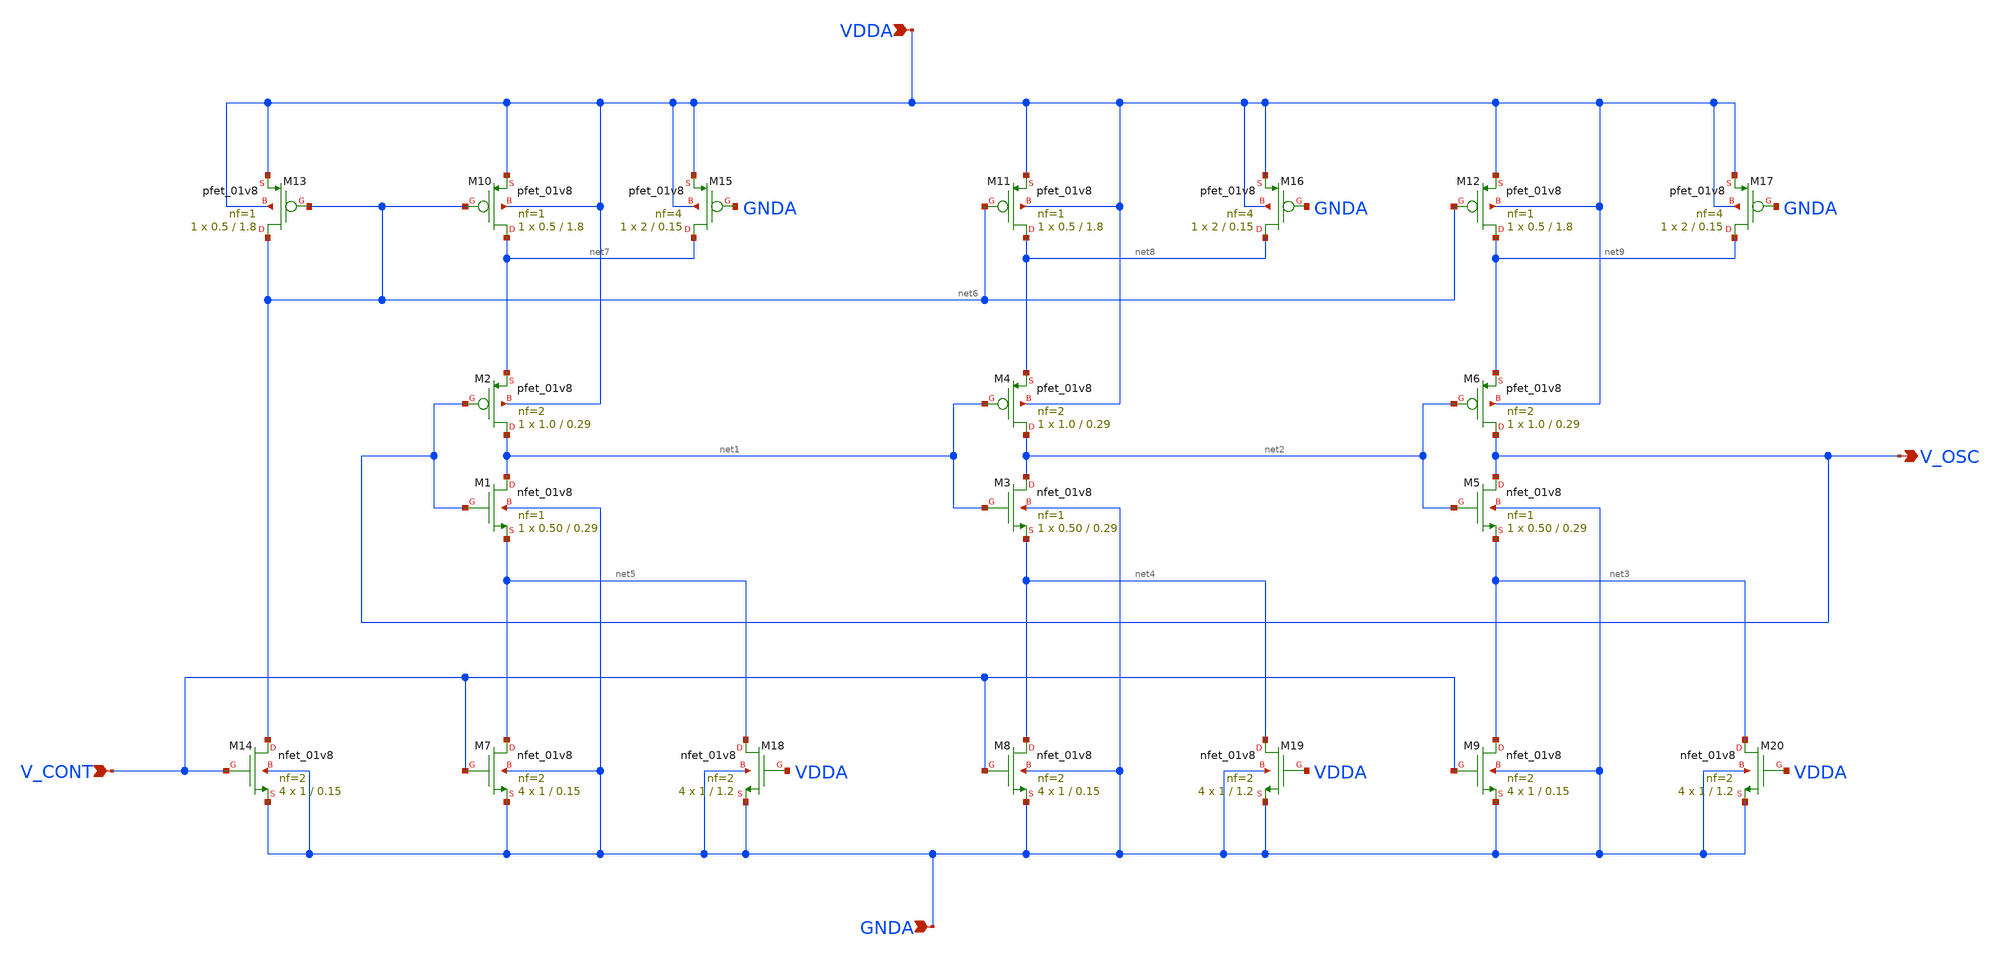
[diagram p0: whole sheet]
** sch_path: projects/pll/vco/xschem_ngspice/current_starved_VCO.sch
**.subckt current_starved_VCO VDDA V_OSC GNDA V_CONT
*.ipin VDDA
*.opin V_OSC
*.ipin GNDA
*.ipin V_CONT
XM1 net1 V_OSC net5 GNDA sky130_fd_pr__nfet_01v8 L=0.29 W=0.50 nf=1 ad='int((nf+1)/2) * W/nf * 0.29'
+ as='int((nf+2)/2) * W/nf * 0.29' pd='2*int((nf+1)/2) * (W/nf + 0.29)' ps='2*int((nf+2)/2) * (W/nf + 0.29)'
+ nrd='0.29 / W' nrs='0.29 / W' sa=0 sb=0 sd=0 mult=1 m=1
XM2 net1 V_OSC net7 VDDA sky130_fd_pr__pfet_01v8 L=0.29 W=1.0 nf=2 ad='int((nf+1)/2) * W/nf * 0.29' as='int((nf+2)/2) * W/nf * 0.29'
+ pd='2*int((nf+1)/2) * (W/nf + 0.29)' ps='2*int((nf+2)/2) * (W/nf + 0.29)' nrd='0.29 / W' nrs='0.29 / W'
+ sa=0 sb=0 sd=0 mult=1 m=1
XM3 net2 net1 net4 GNDA sky130_fd_pr__nfet_01v8 L=0.29 W=0.50 nf=1 ad='int((nf+1)/2) * W/nf * 0.29' as='int((nf+2)/2) * W/nf * 0.29'
+ pd='2*int((nf+1)/2) * (W/nf + 0.29)' ps='2*int((nf+2)/2) * (W/nf + 0.29)' nrd='0.29 / W' nrs='0.29 / W'
+ sa=0 sb=0 sd=0 mult=1 m=1
XM4 net2 net1 net8 VDDA sky130_fd_pr__pfet_01v8 L=0.29 W=1.0 nf=2 ad='int((nf+1)/2) * W/nf * 0.29' as='int((nf+2)/2) * W/nf * 0.29'
+ pd='2*int((nf+1)/2) * (W/nf + 0.29)' ps='2*int((nf+2)/2) * (W/nf + 0.29)' nrd='0.29 / W' nrs='0.29 / W'
+ sa=0 sb=0 sd=0 mult=1 m=1
XM5 V_OSC net2 net3 GNDA sky130_fd_pr__nfet_01v8 L=0.29 W=0.50 nf=1 ad='int((nf+1)/2) * W/nf * 0.29'
+ as='int((nf+2)/2) * W/nf * 0.29' pd='2*int((nf+1)/2) * (W/nf + 0.29)' ps='2*int((nf+2)/2) * (W/nf + 0.29)'
+ nrd='0.29 / W' nrs='0.29 / W' sa=0 sb=0 sd=0 mult=1 m=1
XM6 V_OSC net2 net9 VDDA sky130_fd_pr__pfet_01v8 L=0.29 W=1.0 nf=2 ad='int((nf+1)/2) * W/nf * 0.29' as='int((nf+2)/2) * W/nf * 0.29'
+ pd='2*int((nf+1)/2) * (W/nf + 0.29)' ps='2*int((nf+2)/2) * (W/nf + 0.29)' nrd='0.29 / W' nrs='0.29 / W'
+ sa=0 sb=0 sd=0 mult=1 m=1
XM7 net5 V_CONT GNDA GNDA sky130_fd_pr__nfet_01v8 L=0.15 W=1 nf=2 ad='int((nf+1)/2) * W/nf * 0.29' as='int((nf+2)/2) * W/nf * 0.29'
+ pd='2*int((nf+1)/2) * (W/nf + 0.29)' ps='2*int((nf+2)/2) * (W/nf + 0.29)' nrd='0.29 / W' nrs='0.29 / W'
+ sa=0 sb=0 sd=0 mult=4 m=4
XM8 net4 V_CONT GNDA GNDA sky130_fd_pr__nfet_01v8 L=0.15 W=1 nf=2 ad='int((nf+1)/2) * W/nf * 0.29' as='int((nf+2)/2) * W/nf * 0.29'
+ pd='2*int((nf+1)/2) * (W/nf + 0.29)' ps='2*int((nf+2)/2) * (W/nf + 0.29)' nrd='0.29 / W' nrs='0.29 / W'
+ sa=0 sb=0 sd=0 mult=4 m=4
XM9 net3 V_CONT GNDA GNDA sky130_fd_pr__nfet_01v8 L=0.15 W=1 nf=2 ad='int((nf+1)/2) * W/nf * 0.29' as='int((nf+2)/2) * W/nf * 0.29'
+ pd='2*int((nf+1)/2) * (W/nf + 0.29)' ps='2*int((nf+2)/2) * (W/nf + 0.29)' nrd='0.29 / W' nrs='0.29 / W'
+ sa=0 sb=0 sd=0 mult=4 m=4
XM10 net7 net6 VDDA VDDA sky130_fd_pr__pfet_01v8 L=1.8 W=0.5 nf=1 ad='int((nf+1)/2) * W/nf * 0.29' as='int((nf+2)/2) * W/nf * 0.29'
+ pd='2*int((nf+1)/2) * (W/nf + 0.29)' ps='2*int((nf+2)/2) * (W/nf + 0.29)' nrd='0.29 / W' nrs='0.29 / W'
+ sa=0 sb=0 sd=0 mult=1 m=1
XM11 net8 net6 VDDA VDDA sky130_fd_pr__pfet_01v8 L=1.8 W=0.5 nf=1 ad='int((nf+1)/2) * W/nf * 0.29' as='int((nf+2)/2) * W/nf * 0.29'
+ pd='2*int((nf+1)/2) * (W/nf + 0.29)' ps='2*int((nf+2)/2) * (W/nf + 0.29)' nrd='0.29 / W' nrs='0.29 / W'
+ sa=0 sb=0 sd=0 mult=1 m=1
XM12 net9 net6 VDDA VDDA sky130_fd_pr__pfet_01v8 L=1.8 W=0.5 nf=1 ad='int((nf+1)/2) * W/nf * 0.29' as='int((nf+2)/2) * W/nf * 0.29'
+ pd='2*int((nf+1)/2) * (W/nf + 0.29)' ps='2*int((nf+2)/2) * (W/nf + 0.29)' nrd='0.29 / W' nrs='0.29 / W'
+ sa=0 sb=0 sd=0 mult=1 m=1
XM13 net6 net6 VDDA VDDA sky130_fd_pr__pfet_01v8 L=1.8 W=0.5 nf=1 ad='int((nf+1)/2) * W/nf * 0.29' as='int((nf+2)/2) * W/nf * 0.29'
+ pd='2*int((nf+1)/2) * (W/nf + 0.29)' ps='2*int((nf+2)/2) * (W/nf + 0.29)' nrd='0.29 / W' nrs='0.29 / W'
+ sa=0 sb=0 sd=0 mult=1 m=1
XM14 net6 V_CONT GNDA GNDA sky130_fd_pr__nfet_01v8 L=0.15 W=1 nf=2 ad='int((nf+1)/2) * W/nf * 0.29' as='int((nf+2)/2) * W/nf * 0.29'
+ pd='2*int((nf+1)/2) * (W/nf + 0.29)' ps='2*int((nf+2)/2) * (W/nf + 0.29)' nrd='0.29 / W' nrs='0.29 / W'
+ sa=0 sb=0 sd=0 mult=4 m=4
XM15 net7 GNDA VDDA VDDA sky130_fd_pr__pfet_01v8 L=0.15 W=2 nf=4 ad='int((nf+1)/2) * W/nf * 0.29' as='int((nf+2)/2) * W/nf * 0.29'
+ pd='2*int((nf+1)/2) * (W/nf + 0.29)' ps='2*int((nf+2)/2) * (W/nf + 0.29)' nrd='0.29 / W' nrs='0.29 / W'
+ sa=0 sb=0 sd=0 mult=1 m=1
XM16 net8 GNDA VDDA VDDA sky130_fd_pr__pfet_01v8 L=0.15 W=2 nf=4 ad='int((nf+1)/2) * W/nf * 0.29' as='int((nf+2)/2) * W/nf * 0.29'
+ pd='2*int((nf+1)/2) * (W/nf + 0.29)' ps='2*int((nf+2)/2) * (W/nf + 0.29)' nrd='0.29 / W' nrs='0.29 / W'
+ sa=0 sb=0 sd=0 mult=1 m=1
XM17 net9 GNDA VDDA VDDA sky130_fd_pr__pfet_01v8 L=0.15 W=2 nf=4 ad='int((nf+1)/2) * W/nf * 0.29' as='int((nf+2)/2) * W/nf * 0.29'
+ pd='2*int((nf+1)/2) * (W/nf + 0.29)' ps='2*int((nf+2)/2) * (W/nf + 0.29)' nrd='0.29 / W' nrs='0.29 / W'
+ sa=0 sb=0 sd=0 mult=1 m=1
XM18 net5 VDDA GNDA GNDA sky130_fd_pr__nfet_01v8 L=1.2 W=1 nf=2 ad='int((nf+1)/2) * W/nf * 0.29' as='int((nf+2)/2) * W/nf * 0.29'
+ pd='2*int((nf+1)/2) * (W/nf + 0.29)' ps='2*int((nf+2)/2) * (W/nf + 0.29)' nrd='0.29 / W' nrs='0.29 / W'
+ sa=0 sb=0 sd=0 mult=4 m=4
XM19 net4 VDDA GNDA GNDA sky130_fd_pr__nfet_01v8 L=1.2 W=1 nf=2 ad='int((nf+1)/2) * W/nf * 0.29' as='int((nf+2)/2) * W/nf * 0.29'
+ pd='2*int((nf+1)/2) * (W/nf + 0.29)' ps='2*int((nf+2)/2) * (W/nf + 0.29)' nrd='0.29 / W' nrs='0.29 / W'
+ sa=0 sb=0 sd=0 mult=4 m=4
XM20 net3 VDDA GNDA GNDA sky130_fd_pr__nfet_01v8 L=1.2 W=1 nf=2 ad='int((nf+1)/2) * W/nf * 0.29' as='int((nf+2)/2) * W/nf * 0.29'
+ pd='2*int((nf+1)/2) * (W/nf + 0.29)' ps='2*int((nf+2)/2) * (W/nf + 0.29)' nrd='0.29 / W' nrs='0.29 / W'
+ sa=0 sb=0 sd=0 mult=4 m=4
**.ends
.end
